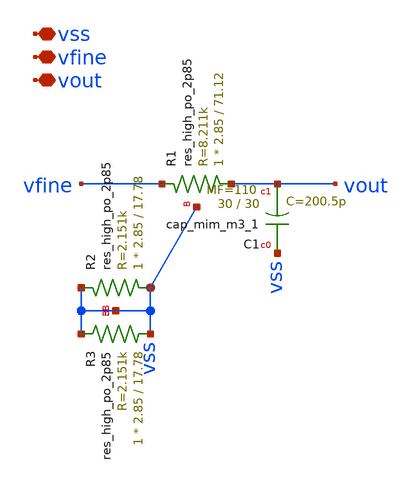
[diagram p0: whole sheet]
** sch_path: xschem/voltage_control.sch
**.subckt voltage_control vss vfine vout
*.iopin vss
*.iopin vfine
*.iopin vout
XC1 vss vout sky130_fd_pr__cap_mim_m3_1 W=30 L=30 MF=110 m=110
XR1 vout vfine vss sky130_fd_pr__res_high_po_2p85 L=71.12 mult=1 m=1
XR2 vss vss vss sky130_fd_pr__res_high_po_2p85 L=17.78 mult=1 m=1
XR3 vss vss vss sky130_fd_pr__res_high_po_2p85 L=17.78 mult=1 m=1
**.ends
.end
